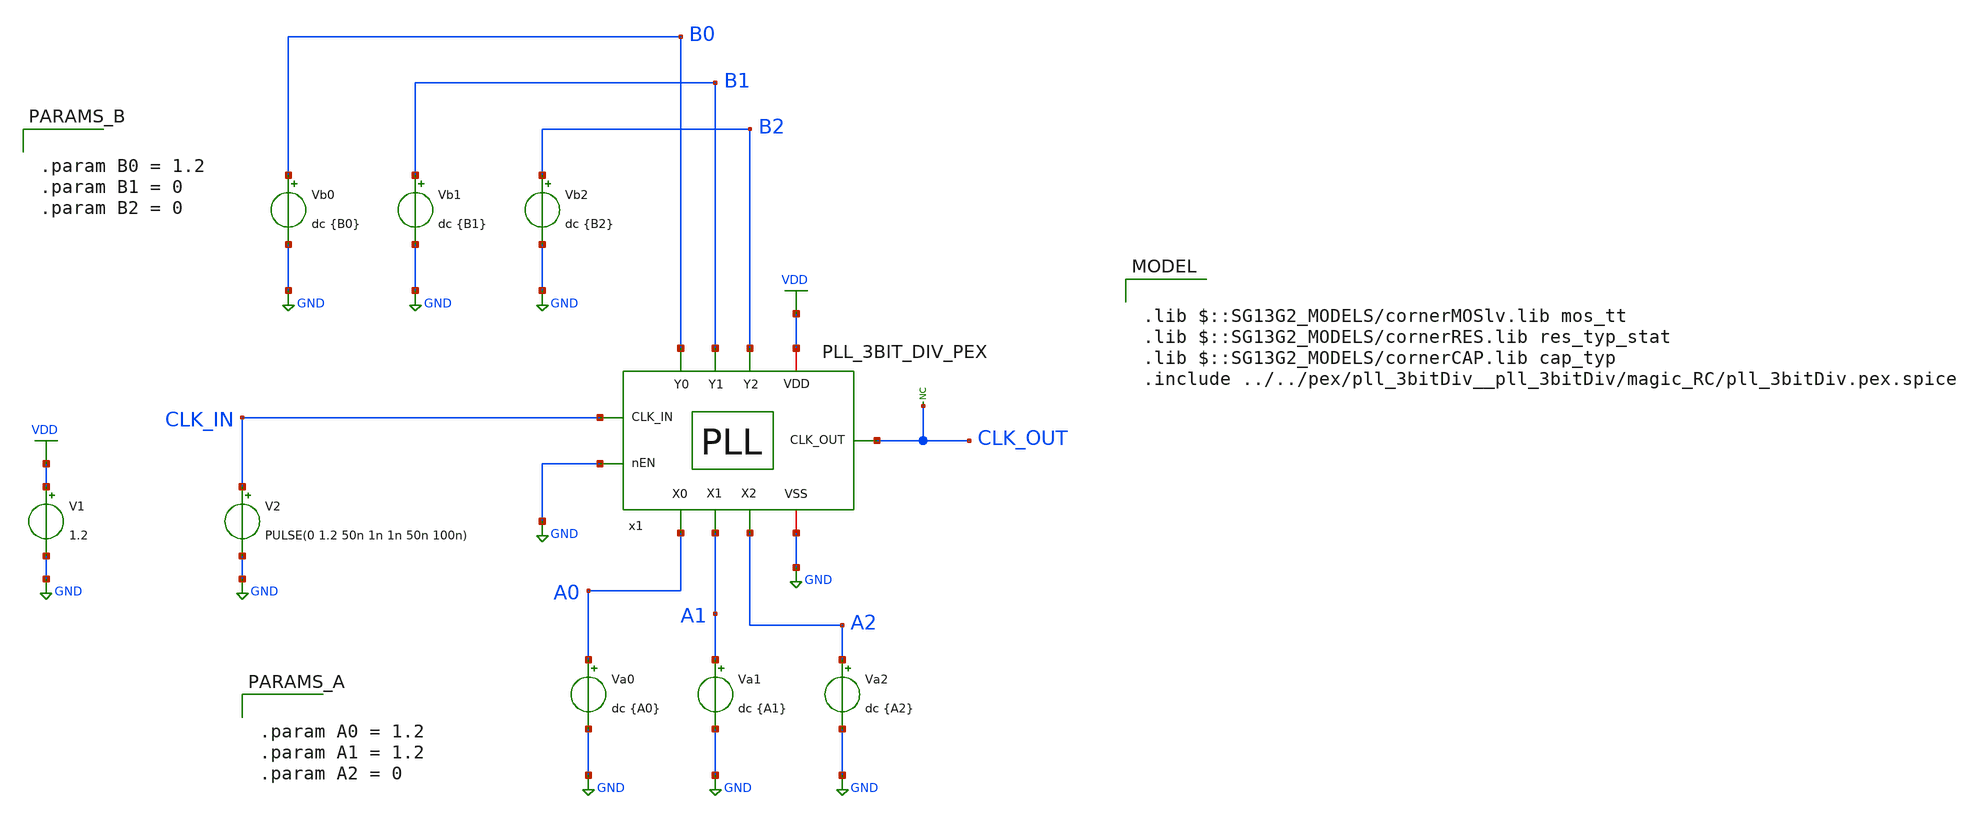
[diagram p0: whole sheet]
** sch_path: 30_MHz_Fractional_N_PLL/design_data/xschem/PLL_3BIT_DIV_PEX_TB.sch

.lib $::SG13G2_MODELS/cornerMOSlv.lib mos_tt
.lib $::SG13G2_MODELS/cornerRES.lib res_typ_stat
.lib $::SG13G2_MODELS/cornerCAP.lib cap_typ
.include ../../pex/pll_3bitDiv__pll_3bitDiv/magic_RC/pll_3bitDiv.pex.spice

**.subckt PLL_3BIT_DIV_PEX_TB
V1 VDD GND 1.2
V2 CLK_IN GND PULSE(0 1.2 50n 1n 1n 50n 100n)
Va0 A0 GND dc {A0}
Va1 A1 GND dc {A1}
* noconn CLK_OUT
Va2 A2 GND dc {A2}
Vb0 B0 GND dc {B0}
Vb1 B1 GND dc {B1}
Vb2 B2 GND dc {B2}
x1 CLK_IN CLK_OUT B0 B2 B1 VDD GND GND A1 A2 A0 PLL_3BIT_DIV_PEX
**** begin user architecture code


.param temp=27
.options klu
.options method=gear gmin=1e-10

*RPUP x1.vco_wob_0.vctl VDD 1e5
*RPDN x1.vco_wob_0.vctl VSS 1e5

.control
save v(x1.PFD_0.UP) v(x1.PFD_0.DOWN) v(clk_in) v(clk_out) v(x1.vco_wob_0.vctl)
+ v(x1.3bit_freq_divider_0.CLK_IN) v(x1.PFD_0.VCO_CLK)
tran 0.1n 10u

write tran_pll_3bitDiv_tb_pex_fmax.raw
.endc





.param A0 = 1.2
.param A1 = 1.2
.param A2 = 0




.param B0 = 1.2
.param B1 = 0
.param B2 = 0




RLEAK_0019 x1.m3_17285_2698# VSS 1e11
RLEAK_0011 x1.a_60922_21818# VSS 1e11
RLEAK_0010 x1.a_60922_21796# VSS 1e11
RLEAK_0005 x1.a_55948_56737# VSS 1e11
RLEAK_0004 x1.a_52808_23573# VSS 1e11
RLEAK_0013 x1.a_60922_23574# VSS 1e11
RLEAK_0024 x1.m6_16847_2260# VSS 1e11
RLEAK_0023 x1.m5_17331_2744# VSS 1e11
RLEAK_0003 x1.a_52808_23551# VSS 1e11
RLEAK_0027 x1.m7_16847_2260# VSS 1e11
RLEAK_0012 x1.a_60922_23552# VSS 1e11
RLEAK_0006 x1.a_56695_49467# VSS 1e11
RLEAK_0017 x1.m2_17285_2698# VSS 1e11
RLEAK_0018 x1.m3_16847_2260# VSS 1e11
RLEAK_0021 x1.m4_17285_2698# VSS 1e11
RLEAK_0001 x1.a_52808_21795# VSS 1e11
RLEAK_0016 x1.m2_16847_2260# VSS 1e11
RLEAK_0022 x1.m5_16847_2260# VSS 1e11
RLEAK_0009 x1.a_60528_49446# VSS 1e11
RLEAK_0020 x1.m4_16847_2260# VSS 1e11
RLEAK_0007 x1.a_56828_53480# VSS 1e11
RLEAK_0014 x1.m1_16847_2260# VSS 1e11
RLEAK_0025 x1.m6_17427_2840# VSS 1e11
RLEAK_0002 x1.a_52808_21817# VSS 1e11
RLEAK_0015 x1.m1_17285_2698# VSS 1e11
RLEAK_0026 x1.m6_60810_42209# VSS 1e11




.ic V(VSS) = 0
.ic V(VDD) = 1.2
*.ic V(B2) = 0
*.ic V(B1) = 0
*.ic V(B0) = 1.2
*.ic V(A2) = 0
*.ic V(A1) = 0
*.ic V(A0) = 1.2
*.ic V(CLK_IN) = 0
.ic V(x1.vco_wob_0.vctl) = 0.6
*.ic V(x1.3bit_freq_divider_1.dff_nclk_0.nCLK) = 1.2
*.ic V(x1.3bit_freq_divider_0.dff_nclk_0.nCLK) = 1.2


**** end user architecture code
**.ends
.GLOBAL GND
.GLOBAL VDD
.end
